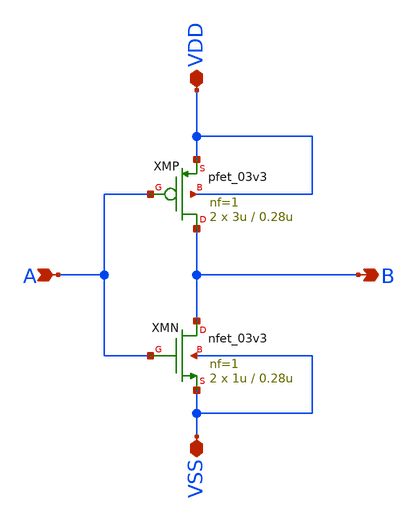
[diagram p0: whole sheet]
** sch_path: designs/DS_modulator/gate_inv_L0d28/xschem/gate_inv_L0d28.sch
**.subckt gate_inv_L0d28 B A VDD VSS
*.opin B
*.ipin A
*.iopin VDD
*.iopin VSS
XMN B A VSS VSS nfet_03v3 L=0.28u W=1u nf=1 ad='int((nf+1)/2) * W/nf * 0.18u' as='int((nf+2)/2) * W/nf * 0.18u'
+ pd='2*int((nf+1)/2) * (W/nf + 0.18u)' ps='2*int((nf+2)/2) * (W/nf + 0.18u)' nrd='0.18u / W' nrs='0.18u / W'
+ sa=0 sb=0 sd=0 m=2
XMP B A VDD VDD pfet_03v3 L=0.28u W=3u nf=1 ad='int((nf+1)/2) * W/nf * 0.18u' as='int((nf+2)/2) * W/nf * 0.18u'
+ pd='2*int((nf+1)/2) * (W/nf + 0.18u)' ps='2*int((nf+2)/2) * (W/nf + 0.18u)' nrd='0.18u / W' nrs='0.18u / W'
+ sa=0 sb=0 sd=0 m=2
**.ends
.end
